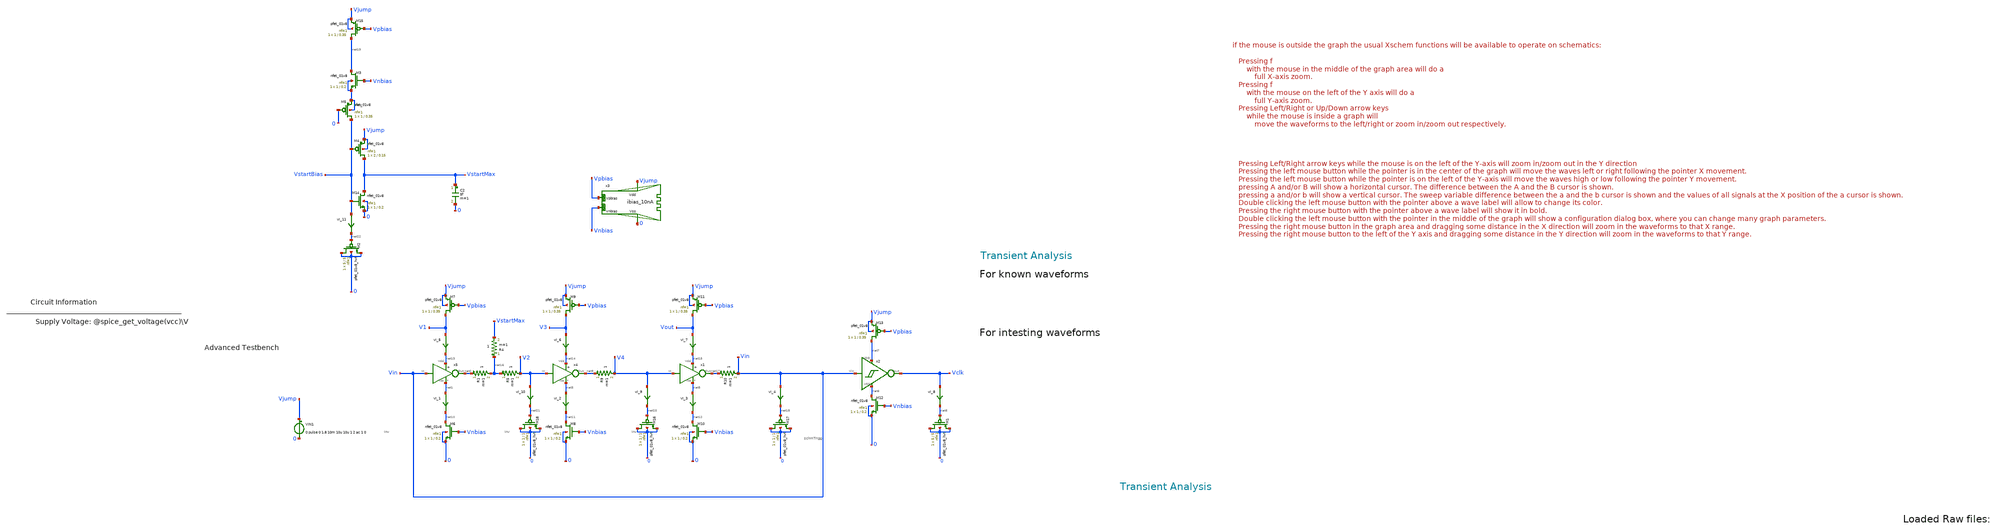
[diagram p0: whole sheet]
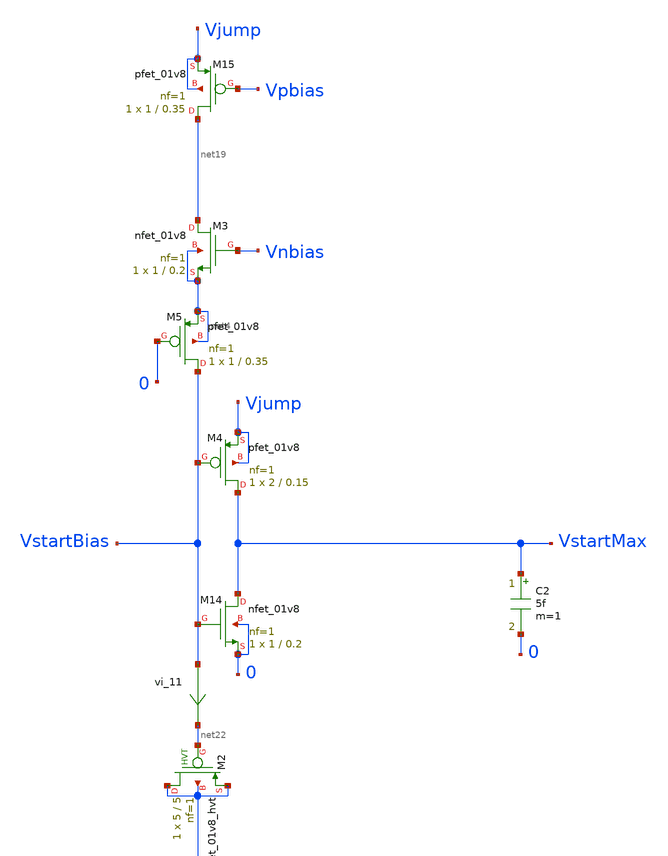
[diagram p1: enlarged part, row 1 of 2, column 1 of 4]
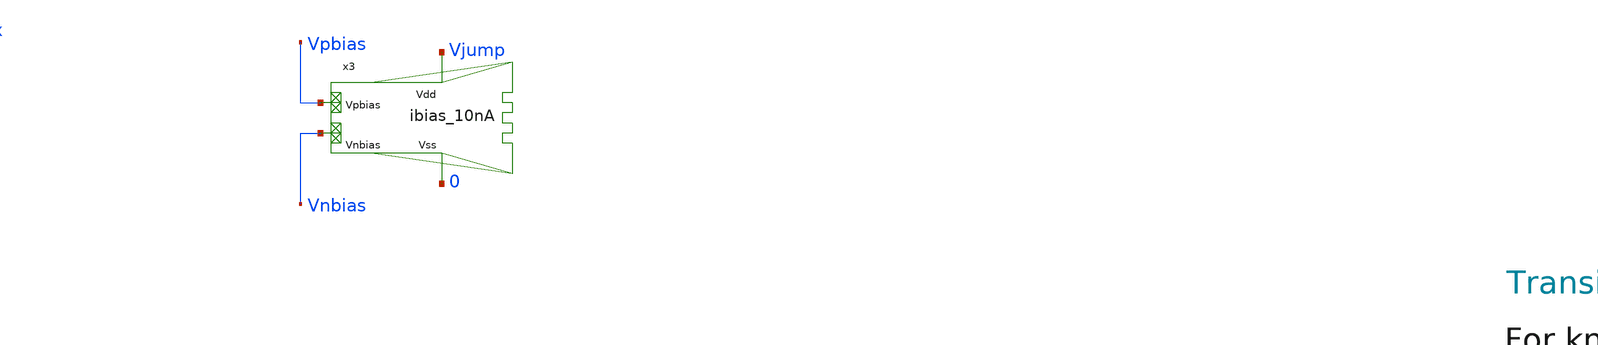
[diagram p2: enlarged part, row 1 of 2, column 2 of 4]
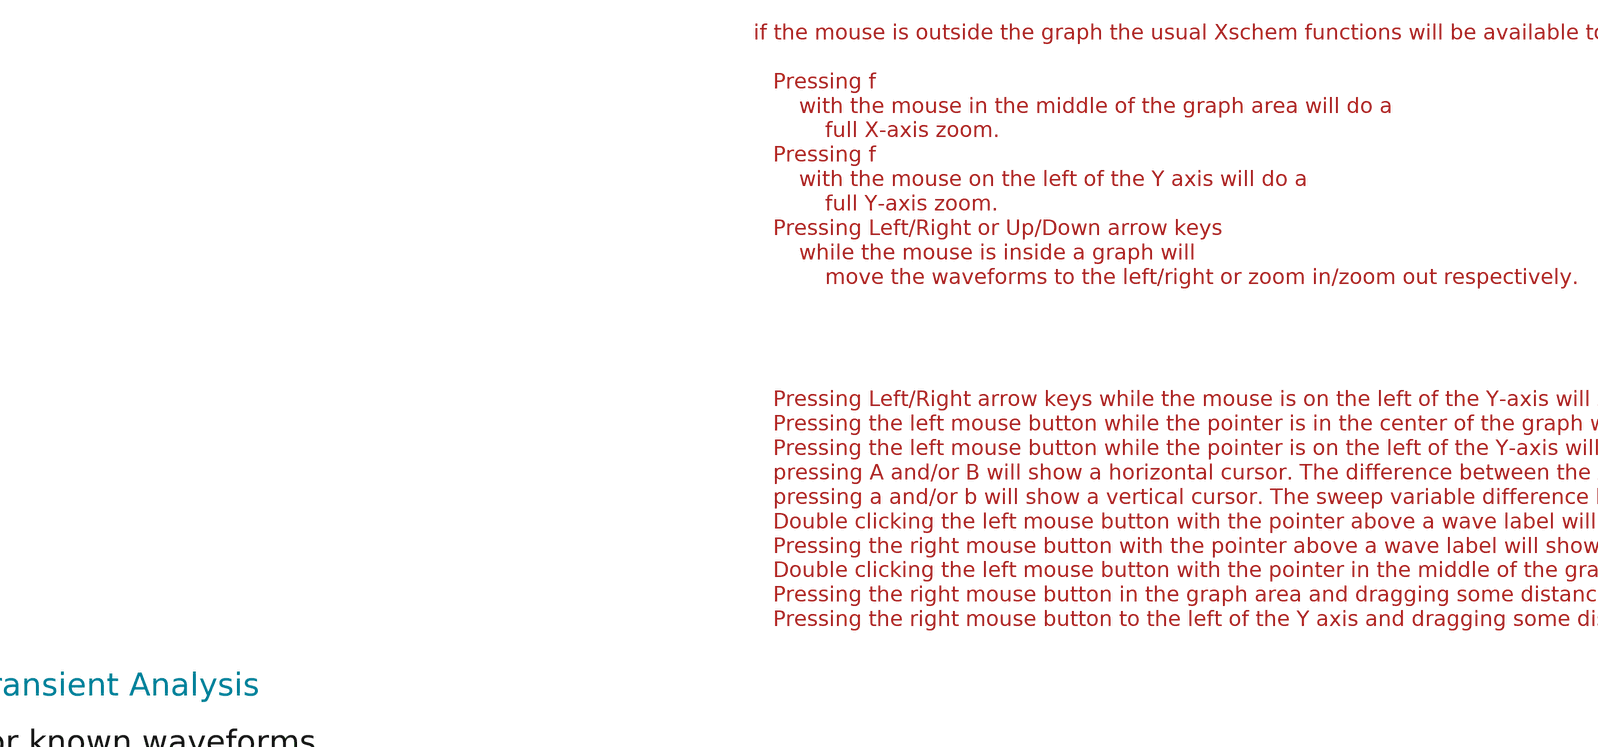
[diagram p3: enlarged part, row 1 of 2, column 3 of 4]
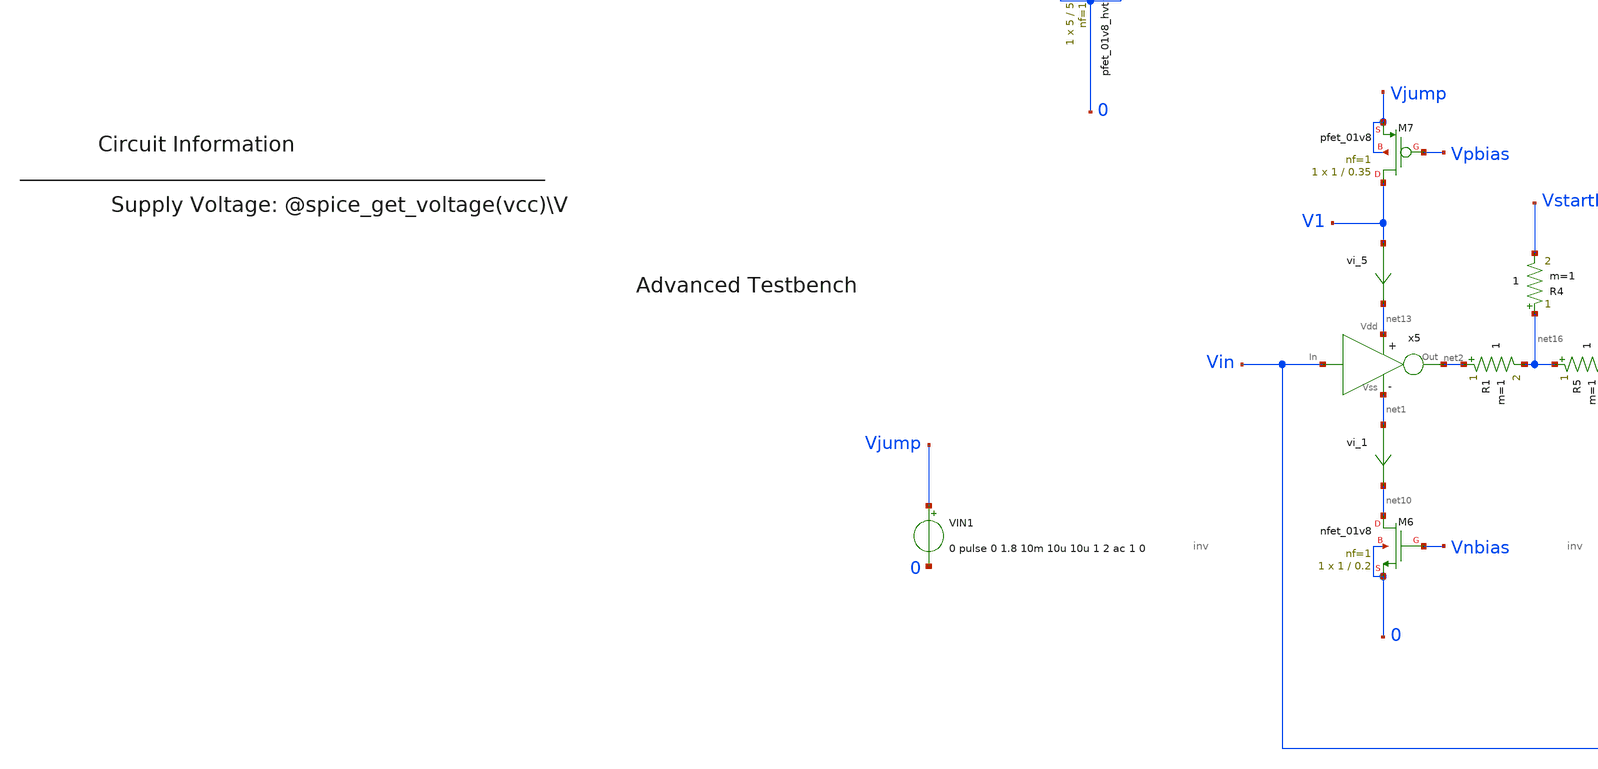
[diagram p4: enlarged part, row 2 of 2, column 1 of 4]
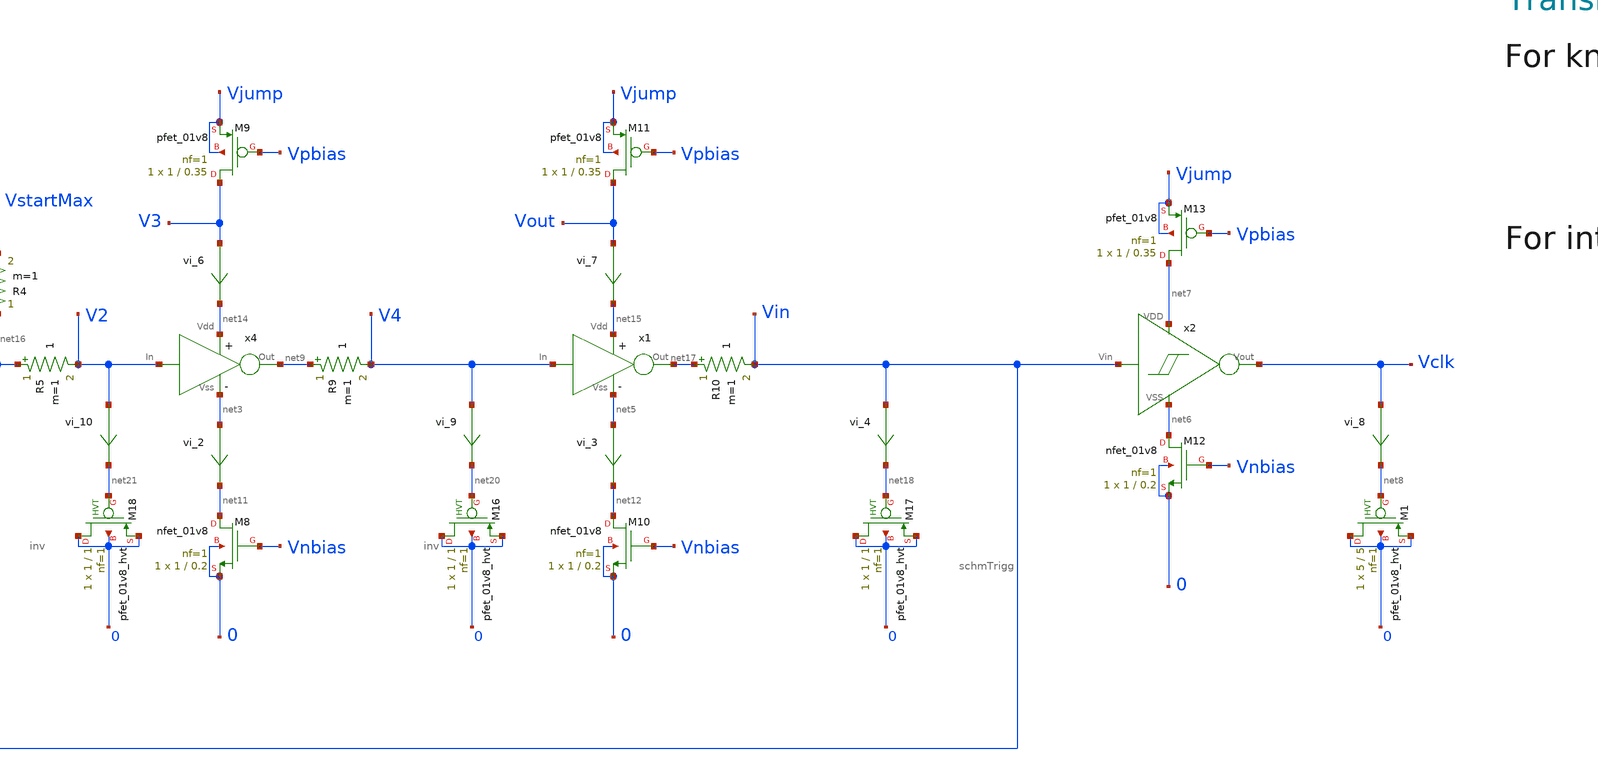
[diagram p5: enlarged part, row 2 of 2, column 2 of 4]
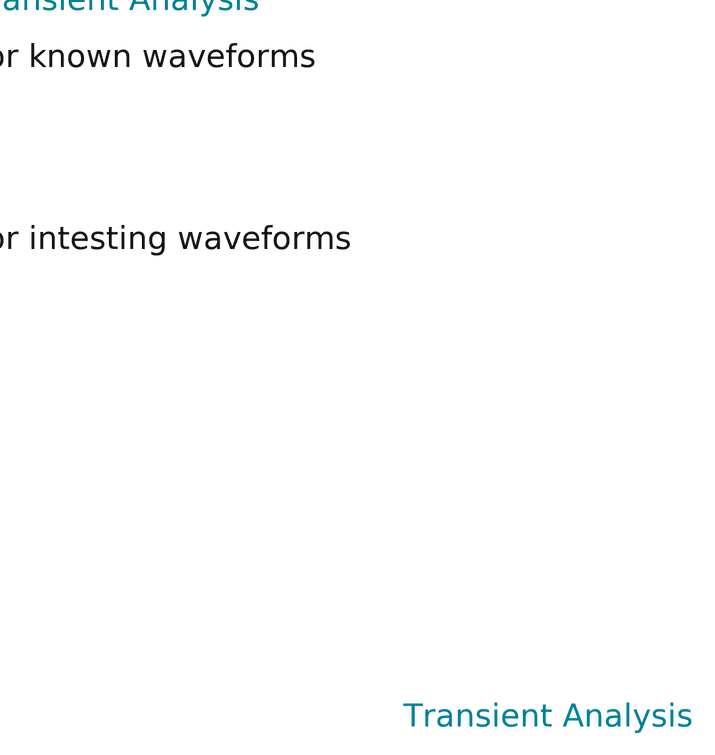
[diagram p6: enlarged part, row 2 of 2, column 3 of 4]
** sch_path: xschem/T3/oscillators/A_tt10_Ring_currentStarved/osc_tb.sch
* Copyright (C) 1998-2024 Stefan Frederik Schippers
* This program is free software; you can redistribute it and/or modify
* it under the terms of the GNU General Public License as published by
* the Free Software Foundation; either version 2 of the License, or
* (at your option) any later version.
* This program is distributed in the hope that it will be useful,
* but WITHOUT ANY WARRANTY; without even the implied warranty of
* MERCHANTABILITY or FITNESS FOR A PARTICULAR PURPOSE.  See the
* GNU General Public License for more details.
* You should have received a copy of the GNU General Public License
* along with this program; if not, write to the Free Software
**.subckt osc_tb
VIN1 Vjump 0 0 pulse 0 1.8 10m 10u 10u 1 2 ac 1 0
R5 net16 V2 1 m=1
R9 net9 V4 1 m=1
x4 net14 net3 net9 V2 inv
x5 net13 net1 net2 Vin inv
XM4 VstartMax VstartBias Vjump Vjump sky130_fd_pr__pfet_01v8 L=0.15 W=2 nf=1 ad='int((nf+1)/2) * W/nf * 0.29'
+ as='int((nf+2)/2) * W/nf * 0.29' pd='2*int((nf+1)/2) * (W/nf + 0.29)' ps='2*int((nf+2)/2) * (W/nf + 0.29)'
+ nrd='0.29 / W' nrs='0.29 / W' sa=0 sb=0 sd=0 mult=1 m=1
XM5 VstartBias 0 net4 net4 sky130_fd_pr__pfet_01v8 L=0.35 W=1 nf=1 ad='int((nf+1)/2) * W/nf * 0.29' as='int((nf+2)/2) * W/nf * 0.29'
+ pd='2*int((nf+1)/2) * (W/nf + 0.29)' ps='2*int((nf+2)/2) * (W/nf + 0.29)' nrd='0.29 / W' nrs='0.29 / W'
+ sa=0 sb=0 sd=0 mult=1 m=1
XM2 0 net22 0 0 sky130_fd_pr__pfet_01v8_hvt L=5 W=5 nf=1 ad='int((1 + 1)/2) * 5 / 1 * 0.29' as='int((1 + 2)/2) * 5 / 1 * 0.29'
+ pd='2*int((1 + 1)/2) * (5 / 1 + 0.29)' ps='2*int((1 + 2)/2) * (5 / 1 + 0.29)' nrd='0.29 / 5 ' nrs='0.29 / 5 '
+ sa=0 sb=0 sd=0 mult=1 m=1
x2 Vin net6 net7 Vclk schmTrigg
x1 net15 net5 net17 V4 inv
x3 Vjump 0 Vnbias Vpbias ibias_10nA
XM6 net10 Vnbias 0 0 sky130_fd_pr__nfet_01v8 L=0.2 W=1 nf=1 ad='int((1 + 1)/2) * 1 / 1 * 0.29' as='int((1 + 2)/2) * 1 / 1 * 0.29'
+ pd='2*int((1 + 1)/2) * (1 / 1 + 0.29)' ps='2*int((1 + 2)/2) * (1 / 1 + 0.29)' nrd='0.29 / 1 ' nrs='0.29 / 1 '
+ sa=0 sb=0 sd=0 mult=1 m=1
XM7 V1 Vpbias Vjump Vjump sky130_fd_pr__pfet_01v8 L=0.35 W=1 nf=1 ad='int((nf+1)/2) * W/nf * 0.29' as='int((nf+2)/2) * W/nf * 0.29'
+ pd='2*int((nf+1)/2) * (W/nf + 0.29)' ps='2*int((nf+2)/2) * (W/nf + 0.29)' nrd='0.29 / W' nrs='0.29 / W'
+ sa=0 sb=0 sd=0 mult=1 m=1
XM8 net11 Vnbias 0 0 sky130_fd_pr__nfet_01v8 L=0.2 W=1 nf=1 ad='int((1 + 1)/2) * 1 / 1 * 0.29' as='int((1 + 2)/2) * 1 / 1 * 0.29'
+ pd='2*int((1 + 1)/2) * (1 / 1 + 0.29)' ps='2*int((1 + 2)/2) * (1 / 1 + 0.29)' nrd='0.29 / 1 ' nrs='0.29 / 1 '
+ sa=0 sb=0 sd=0 mult=1 m=1
XM9 V3 Vpbias Vjump Vjump sky130_fd_pr__pfet_01v8 L=0.35 W=1 nf=1 ad='int((nf+1)/2) * W/nf * 0.29' as='int((nf+2)/2) * W/nf * 0.29'
+ pd='2*int((nf+1)/2) * (W/nf + 0.29)' ps='2*int((nf+2)/2) * (W/nf + 0.29)' nrd='0.29 / W' nrs='0.29 / W'
+ sa=0 sb=0 sd=0 mult=1 m=1
XM10 net12 Vnbias 0 0 sky130_fd_pr__nfet_01v8 L=0.2 W=1 nf=1 ad='int((1 + 1)/2) * 1 / 1 * 0.29' as='int((1 + 2)/2) * 1 / 1 * 0.29'
+ pd='2*int((1 + 1)/2) * (1 / 1 + 0.29)' ps='2*int((1 + 2)/2) * (1 / 1 + 0.29)' nrd='0.29 / 1 ' nrs='0.29 / 1 '
+ sa=0 sb=0 sd=0 mult=1 m=1
XM11 Vout Vpbias Vjump Vjump sky130_fd_pr__pfet_01v8 L=0.35 W=1 nf=1 ad='int((nf+1)/2) * W/nf * 0.29'
+ as='int((nf+2)/2) * W/nf * 0.29' pd='2*int((nf+1)/2) * (W/nf + 0.29)' ps='2*int((nf+2)/2) * (W/nf + 0.29)'
+ nrd='0.29 / W' nrs='0.29 / W' sa=0 sb=0 sd=0 mult=1 m=1
XM12 net6 Vnbias 0 0 sky130_fd_pr__nfet_01v8 L=0.2 W=1 nf=1 ad='int((1 + 1)/2) * 1 / 1 * 0.29' as='int((1 + 2)/2) * 1 / 1 * 0.29'
+ pd='2*int((1 + 1)/2) * (1 / 1 + 0.29)' ps='2*int((1 + 2)/2) * (1 / 1 + 0.29)' nrd='0.29 / 1 ' nrs='0.29 / 1 '
+ sa=0 sb=0 sd=0 mult=1 m=1
XM13 net7 Vpbias Vjump Vjump sky130_fd_pr__pfet_01v8 L=0.35 W=1 nf=1 ad='int((nf+1)/2) * W/nf * 0.29'
+ as='int((nf+2)/2) * W/nf * 0.29' pd='2*int((nf+1)/2) * (W/nf + 0.29)' ps='2*int((nf+2)/2) * (W/nf + 0.29)'
+ nrd='0.29 / W' nrs='0.29 / W' sa=0 sb=0 sd=0 mult=1 m=1
XM15 net19 Vpbias Vjump Vjump sky130_fd_pr__pfet_01v8 L=0.35 W=1 nf=1 ad='int((nf+1)/2) * W/nf * 0.29'
+ as='int((nf+2)/2) * W/nf * 0.29' pd='2*int((nf+1)/2) * (W/nf + 0.29)' ps='2*int((nf+2)/2) * (W/nf + 0.29)'
+ nrd='0.29 / W' nrs='0.29 / W' sa=0 sb=0 sd=0 mult=1 m=1
vi_1 net1 net10 0
.save i(vi_1)
XM1 0 net8 0 0 sky130_fd_pr__pfet_01v8_hvt L=5 W=5 nf=1 ad='int((1 + 1)/2) * 5 / 1 * 0.29' as='int((1 + 2)/2) * 5 / 1 * 0.29'
+ pd='2*int((1 + 1)/2) * (5 / 1 + 0.29)' ps='2*int((1 + 2)/2) * (5 / 1 + 0.29)' nrd='0.29 / 5 ' nrs='0.29 / 5 '
+ sa=0 sb=0 sd=0 mult=1 m=1
C2 VstartMax 0 5f m=1
R4 net16 VstartMax 1 m=1
R10 net17 Vin 1 m=1
XM17 0 net18 0 0 sky130_fd_pr__pfet_01v8_hvt L=1 W=1 nf=1 ad='int((1 + 1)/2) * 1 / 1 * 0.29' as='int((1 + 2)/2) * 1 / 1 * 0.29'
+ pd='2*int((1 + 1)/2) * (1 / 1 + 0.29)' ps='2*int((1 + 2)/2) * (1 / 1 + 0.29)' nrd='0.29 / 1 ' nrs='0.29 / 1 '
+ sa=0 sb=0 sd=0 mult=1 m=1
vi_2 net3 net11 0
.save i(vi_2)
vi_3 net5 net12 0
.save i(vi_3)
vi_4 Vin net18 0
.save i(vi_4)
vi_5 V1 net13 0
.save i(vi_5)
vi_6 V3 net14 0
.save i(vi_6)
vi_7 Vout net15 0
.save i(vi_7)
vi_8 Vclk net8 0
.save i(vi_8)
XM3 net19 Vnbias net4 net4 sky130_fd_pr__nfet_01v8 L=0.2 W=1 nf=1 ad='int((1 + 1)/2) * 1 / 1 * 0.29'
+ as='int((1 + 2)/2) * 1 / 1 * 0.29' pd='2*int((1 + 1)/2) * (1 / 1 + 0.29)' ps='2*int((1 + 2)/2) * (1 / 1 + 0.29)'
+ nrd='0.29 / 1 ' nrs='0.29 / 1 ' sa=0 sb=0 sd=0 mult=1 m=1
XM14 VstartMax VstartBias 0 0 sky130_fd_pr__nfet_01v8 L=0.2 W=1 nf=1 ad='int((1 + 1)/2) * 1 / 1 * 0.29'
+ as='int((1 + 2)/2) * 1 / 1 * 0.29' pd='2*int((1 + 1)/2) * (1 / 1 + 0.29)' ps='2*int((1 + 2)/2) * (1 / 1 + 0.29)'
+ nrd='0.29 / 1 ' nrs='0.29 / 1 ' sa=0 sb=0 sd=0 mult=1 m=1
XM16 0 net20 0 0 sky130_fd_pr__pfet_01v8_hvt L=1 W=1 nf=1 ad='int((1 + 1)/2) * 1 / 1 * 0.29' as='int((1 + 2)/2) * 1 / 1 * 0.29'
+ pd='2*int((1 + 1)/2) * (1 / 1 + 0.29)' ps='2*int((1 + 2)/2) * (1 / 1 + 0.29)' nrd='0.29 / 1 ' nrs='0.29 / 1 '
+ sa=0 sb=0 sd=0 mult=1 m=1
vi_9 V4 net20 0
.save i(vi_9)
XM18 0 net21 0 0 sky130_fd_pr__pfet_01v8_hvt L=1 W=1 nf=1 ad='int((1 + 1)/2) * 1 / 1 * 0.29' as='int((1 + 2)/2) * 1 / 1 * 0.29'
+ pd='2*int((1 + 1)/2) * (1 / 1 + 0.29)' ps='2*int((1 + 2)/2) * (1 / 1 + 0.29)' nrd='0.29 / 1 ' nrs='0.29 / 1 '
+ sa=0 sb=0 sd=0 mult=1 m=1
vi_10 V2 net21 0
.save i(vi_10)
vi_11 VstartBias net22 0
.save i(vi_11)
R1 net2 net16 1 m=1
**** begin user architecture code



.temp 30
.param Vdd = 1.8
.param imax = 600e-9
.param var_cap = 1p
.param var_res = 7000k


.option savecurrents
.save all @m14[gm]
.control
  save all alli
  save @m.xm14.msky130_fd_pr__nfet_01v8[gm]

  op
  let power=-v(vcc) * i(vvcc)
  settype power power
  write template_adv_tb.raw
  set appendwrite


  tran 100u 300m
  write template_adv_tb.raw





  quit 0




.endc





** opencircuitdesign pdks install
.lib $::SKYWATER_MODELS/sky130.lib.spice tt


**** end user architecture code
**.ends

* expanding   symbol:  T0/inv/inv.sym # of pins=4
** sym_path: xschem/T0/inv/inv.sym
** sch_path: xschem/T0/inv/inv.sch
.subckt inv Vdd Vss Out In
*.ipin Vdd
*.ipin Vss
*.opin Out
*.ipin In
XM1 Out In Vss Vss sky130_fd_pr__nfet_01v8 L=0.15 W=1 nf=1 ad='int((1 + 1)/2) * 1 / 1 * 0.29' as='int((1 + 2)/2) * 1 / 1 * 0.29'
+ pd='2*int((1 + 1)/2) * (1 / 1 + 0.29)' ps='2*int((1 + 2)/2) * (1 / 1 + 0.29)' nrd='0.29 / 1 ' nrs='0.29 / 1 '
+ sa=0 sb=0 sd=0 mult=1 m=1
XM2 Out In Vdd Vdd sky130_fd_pr__pfet_01v8 L=0.15 W=1 nf=1 ad='int((nf+1)/2) * W/nf * 0.29' as='int((nf+2)/2) * W/nf * 0.29'
+ pd='2*int((nf+1)/2) * (W/nf + 0.29)' ps='2*int((nf+2)/2) * (W/nf + 0.29)' nrd='0.29 / W' nrs='0.29 / W'
+ sa=0 sb=0 sd=0 mult=1 m=1
.ends


* expanding   symbol:  T1/schmTrigg/schmTrigg.sym # of pins=4
** sym_path: xschem/T1/schmTrigg/schmTrigg.sym
** sch_path: xschem/T1/schmTrigg/schmTrigg.sch
.subckt schmTrigg Vin VSS VDD Vout
*.ipin Vin
*.ipin VDD
*.ipin VSS
*.opin Vout
XM1 VDD Vout Vn Vn sky130_fd_pr__nfet_01v8 L=0.15 W=1 nf=1 ad='int((1 + 1)/2) * 1 / 1 * 0.29' as='int((1 + 2)/2) * 1 / 1 * 0.29'
+ pd='2*int((1 + 1)/2) * (1 / 1 + 0.29)' ps='2*int((1 + 2)/2) * (1 / 1 + 0.29)' nrd='0.29 / 1 ' nrs='0.29 / 1 '
+ sa=0 sb=0 sd=0 mult=1 m=1
XM2 Vn Vin VSS VSS sky130_fd_pr__nfet_01v8 L=0.15 W=1 nf=1 ad='int((1 + 1)/2) * 1 / 1 * 0.29' as='int((1 + 2)/2) * 1 / 1 * 0.29'
+ pd='2*int((1 + 1)/2) * (1 / 1 + 0.29)' ps='2*int((1 + 2)/2) * (1 / 1 + 0.29)' nrd='0.29 / 1 ' nrs='0.29 / 1 '
+ sa=0 sb=0 sd=0 mult=1 m=1
XM3 Vout Vin Vn Vn sky130_fd_pr__nfet_01v8 L=0.15 W=1 nf=1 ad='int((1 + 1)/2) * 1 / 1 * 0.29' as='int((1 + 2)/2) * 1 / 1 * 0.29'
+ pd='2*int((1 + 1)/2) * (1 / 1 + 0.29)' ps='2*int((1 + 2)/2) * (1 / 1 + 0.29)' nrd='0.29 / 1 ' nrs='0.29 / 1 '
+ sa=0 sb=0 sd=0 mult=1 m=1
XM4 VSS Vout Vp Vp sky130_fd_pr__pfet_01v8 L=0.15 W=1 nf=1 ad='int((nf+1)/2) * W/nf * 0.29' as='int((nf+2)/2) * W/nf * 0.29'
+ pd='2*int((nf+1)/2) * (W/nf + 0.29)' ps='2*int((nf+2)/2) * (W/nf + 0.29)' nrd='0.29 / W' nrs='0.29 / W'
+ sa=0 sb=0 sd=0 mult=1 m=1
XM5 Vout Vin Vp Vp sky130_fd_pr__pfet_01v8 L=0.15 W=1 nf=1 ad='int((nf+1)/2) * W/nf * 0.29' as='int((nf+2)/2) * W/nf * 0.29'
+ pd='2*int((nf+1)/2) * (W/nf + 0.29)' ps='2*int((nf+2)/2) * (W/nf + 0.29)' nrd='0.29 / W' nrs='0.29 / W'
+ sa=0 sb=0 sd=0 mult=1 m=1
XM6 Vp Vin VDD VDD sky130_fd_pr__pfet_01v8 L=0.15 W=1 nf=1 ad='int((nf+1)/2) * W/nf * 0.29' as='int((nf+2)/2) * W/nf * 0.29'
+ pd='2*int((nf+1)/2) * (W/nf + 0.29)' ps='2*int((nf+2)/2) * (W/nf + 0.29)' nrd='0.29 / W' nrs='0.29 / W'
+ sa=0 sb=0 sd=0 mult=1 m=1
.ends


* expanding   symbol:  T2/biasGen/A_tt10_10nA/ibias_10nA.sym # of pins=4
** sym_path: T2/biasGen/A_tt10_10nA/ibias_10nA.sym
** sch_path: T2/biasGen/A_tt10_10nA/ibias_10nA.sch
.subckt ibias_10nA Vdd Vss Vnbias Vpbias
*.ipin Vdd
*.ipin Vss
*.opin Vnbias
*.opin Vpbias
XM56 Vpbias Vpbias Vdd Vdd sky130_fd_pr__pfet_01v8 L=0.35 W=1 nf=1 ad='int((nf+1)/2) * W/nf * 0.29' as='int((nf+2)/2) * W/nf * 0.29'
+ pd='2*int((nf+1)/2) * (W/nf + 0.29)' ps='2*int((nf+2)/2) * (W/nf + 0.29)' nrd='0.29 / W' nrs='0.29 / W'
+ sa=0 sb=0 sd=0 mult=1 m=1
XM57 Vnbias Vpbias Vdd Vdd sky130_fd_pr__pfet_01v8 L=0.35 W=1 nf=1 ad='int((nf+1)/2) * W/nf * 0.29' as='int((nf+2)/2) * W/nf * 0.29'
+ pd='2*int((nf+1)/2) * (W/nf + 0.29)' ps='2*int((nf+2)/2) * (W/nf + 0.29)' nrd='0.29 / W' nrs='0.29 / W'
+ sa=0 sb=0 sd=0 mult=1 m=1
XM58 net2 Vpbias Vdd Vdd sky130_fd_pr__pfet_01v8 L=0.30 W=2 nf=1 ad='int((nf+1)/2) * W/nf * 0.29' as='int((nf+2)/2) * W/nf * 0.29'
+ pd='2*int((nf+1)/2) * (W/nf + 0.29)' ps='2*int((nf+2)/2) * (W/nf + 0.29)' nrd='0.29 / W' nrs='0.29 / W'
+ sa=0 sb=0 sd=0 mult=1 m=1
XM59 Vpbias Vnbias net1 net1 sky130_fd_pr__nfet_01v8 L=0.2 W=1 nf=1 ad='int((1 + 1)/2) * 1 / 1 * 0.29'
+ as='int((1 + 2)/2) * 1 / 1 * 0.29' pd='2*int((1 + 1)/2) * (1 / 1 + 0.29)' ps='2*int((1 + 2)/2) * (1 / 1 + 0.29)'
+ nrd='0.29 / 1 ' nrs='0.29 / 1 ' sa=0 sb=0 sd=0 mult=1 m=1
XM60 Vnbias Vnbias Vss Vss sky130_fd_pr__nfet_01v8 L=0.2 W=1 nf=1 ad='int((1 + 1)/2) * 1 / 1 * 0.29'
+ as='int((1 + 2)/2) * 1 / 1 * 0.29' pd='2*int((1 + 1)/2) * (1 / 1 + 0.29)' ps='2*int((1 + 2)/2) * (1 / 1 + 0.29)'
+ nrd='0.29 / 1 ' nrs='0.29 / 1 ' sa=0 sb=0 sd=0 mult=1 m=1
XM61 net2 net2 net1 net1 sky130_fd_pr__nfet_01v8 L=0.2 W=1 nf=1 ad='int((1 + 1)/2) * 1 / 1 * 0.29' as='int((1 + 2)/2) * 1 / 1 * 0.29'
+ pd='2*int((1 + 1)/2) * (1 / 1 + 0.29)' ps='2*int((1 + 2)/2) * (1 / 1 + 0.29)' nrd='0.29 / 1 ' nrs='0.29 / 1 '
+ sa=0 sb=0 sd=0 mult=1 m=1
XM62 net1 net2 Vss Vss sky130_fd_pr__nfet_01v8 L=1 W=1 nf=1 ad='int((1 + 1)/2) * 1 / 1 * 0.29' as='int((1 + 2)/2) * 1 / 1 * 0.29'
+ pd='2*int((1 + 1)/2) * (1 / 1 + 0.29)' ps='2*int((1 + 2)/2) * (1 / 1 + 0.29)' nrd='0.29 / 1 ' nrs='0.29 / 1 '
+ sa=0 sb=0 sd=0 mult=1 m=1
.ends

.end
